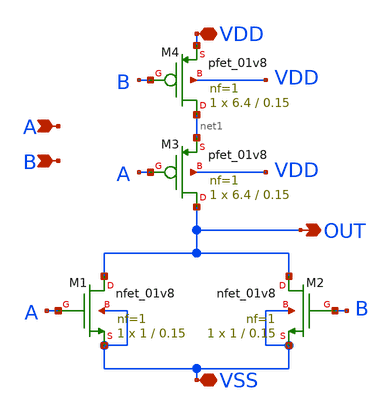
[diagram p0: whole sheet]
** sch_path: design/ALU/nor2.sch
**.subckt nor2 A B VSS VDD OUT
*.ipin A
*.ipin B
*.iopin VSS
*.iopin VDD
*.opin OUT
XM3 OUT A net1 VDD sky130_fd_pr__pfet_01v8 L=0.15 W=6.4 nf=1 ad='int((nf+1)/2) * W/nf * 0.29' as='int((nf+2)/2) * W/nf * 0.29'
+ pd='2*int((nf+1)/2) * (W/nf + 0.29)' ps='2*int((nf+2)/2) * (W/nf + 0.29)' nrd='0.29 / W' nrs='0.29 / W'
+ sa=0 sb=0 sd=0 mult=1 m=1
XM4 net1 B VDD VDD sky130_fd_pr__pfet_01v8 L=0.15 W=6.4 nf=1 ad='int((nf+1)/2) * W/nf * 0.29' as='int((nf+2)/2) * W/nf * 0.29'
+ pd='2*int((nf+1)/2) * (W/nf + 0.29)' ps='2*int((nf+2)/2) * (W/nf + 0.29)' nrd='0.29 / W' nrs='0.29 / W'
+ sa=0 sb=0 sd=0 mult=1 m=1
XM1 OUT A VSS VSS sky130_fd_pr__nfet_01v8 L=0.15 W=1 nf=1 ad='int((nf+1)/2) * W/nf * 0.29' as='int((nf+2)/2) * W/nf * 0.29'
+ pd='2*int((nf+1)/2) * (W/nf + 0.29)' ps='2*int((nf+2)/2) * (W/nf + 0.29)' nrd='0.29 / W' nrs='0.29 / W'
+ sa=0 sb=0 sd=0 mult=1 m=1
XM2 OUT B VSS VSS sky130_fd_pr__nfet_01v8 L=0.15 W=1 nf=1 ad='int((nf+1)/2) * W/nf * 0.29' as='int((nf+2)/2) * W/nf * 0.29'
+ pd='2*int((nf+1)/2) * (W/nf + 0.29)' ps='2*int((nf+2)/2) * (W/nf + 0.29)' nrd='0.29 / W' nrs='0.29 / W'
+ sa=0 sb=0 sd=0 mult=1 m=1
**.ends
.end
